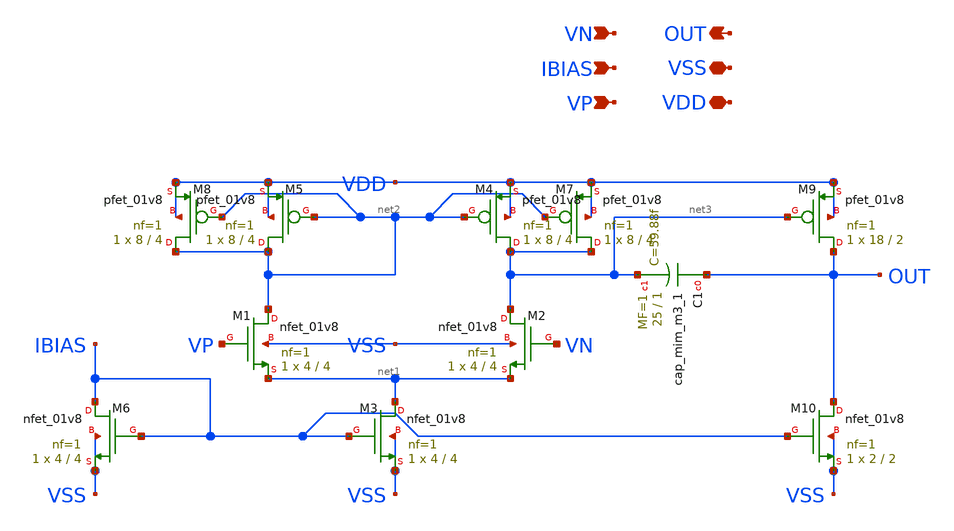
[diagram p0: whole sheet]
** sch_path: designs/libs/core_analog/core_bandgap/5t-ota/n-ota-bg.sch
**.subckt n-ota-bg VDD VSS IBIAS VP VN OUT
*.iopin VDD
*.iopin VSS
*.ipin IBIAS
*.ipin VP
*.ipin VN
*.opin OUT
XM1 net2 VP net1 VSS sky130_fd_pr__nfet_01v8 L=4 W=4 nf=1 ad='int((nf+1)/2) * W/nf * 0.29' as='int((nf+2)/2) * W/nf * 0.29'
+ pd='2*int((nf+1)/2) * (W/nf + 0.29)' ps='2*int((nf+2)/2) * (W/nf + 0.29)' nrd='0.29 / W' nrs='0.29 / W'
+ sa=0 sb=0 sd=0 mult=1 m=1
XM2 net3 VN net1 VSS sky130_fd_pr__nfet_01v8 L=4 W=4 nf=1 ad='int((nf+1)/2) * W/nf * 0.29' as='int((nf+2)/2) * W/nf * 0.29'
+ pd='2*int((nf+1)/2) * (W/nf + 0.29)' ps='2*int((nf+2)/2) * (W/nf + 0.29)' nrd='0.29 / W' nrs='0.29 / W'
+ sa=0 sb=0 sd=0 mult=1 m=1
XM3 net1 IBIAS VSS VSS sky130_fd_pr__nfet_01v8 L=4 W=4 nf=1 ad='int((nf+1)/2) * W/nf * 0.29' as='int((nf+2)/2) * W/nf * 0.29'
+ pd='2*int((nf+1)/2) * (W/nf + 0.29)' ps='2*int((nf+2)/2) * (W/nf + 0.29)' nrd='0.29 / W' nrs='0.29 / W'
+ sa=0 sb=0 sd=0 mult=1 m=1
XM4 net3 net2 VDD VDD sky130_fd_pr__pfet_01v8 L=4 W=8 nf=1 ad='int((nf+1)/2) * W/nf * 0.29' as='int((nf+2)/2) * W/nf * 0.29'
+ pd='2*int((nf+1)/2) * (W/nf + 0.29)' ps='2*int((nf+2)/2) * (W/nf + 0.29)' nrd='0.29 / W' nrs='0.29 / W'
+ sa=0 sb=0 sd=0 mult=1 m=1
XM5 net2 net2 VDD VDD sky130_fd_pr__pfet_01v8 L=4 W=8 nf=1 ad='int((nf+1)/2) * W/nf * 0.29' as='int((nf+2)/2) * W/nf * 0.29'
+ pd='2*int((nf+1)/2) * (W/nf + 0.29)' ps='2*int((nf+2)/2) * (W/nf + 0.29)' nrd='0.29 / W' nrs='0.29 / W'
+ sa=0 sb=0 sd=0 mult=1 m=1
XM6 IBIAS IBIAS VSS VSS sky130_fd_pr__nfet_01v8 L=4 W=4 nf=1 ad='int((nf+1)/2) * W/nf * 0.29' as='int((nf+2)/2) * W/nf * 0.29'
+ pd='2*int((nf+1)/2) * (W/nf + 0.29)' ps='2*int((nf+2)/2) * (W/nf + 0.29)' nrd='0.29 / W' nrs='0.29 / W'
+ sa=0 sb=0 sd=0 mult=1 m=1
XM7 net3 net2 VDD VDD sky130_fd_pr__pfet_01v8 L=4 W=8 nf=1 ad='int((nf+1)/2) * W/nf * 0.29' as='int((nf+2)/2) * W/nf * 0.29'
+ pd='2*int((nf+1)/2) * (W/nf + 0.29)' ps='2*int((nf+2)/2) * (W/nf + 0.29)' nrd='0.29 / W' nrs='0.29 / W'
+ sa=0 sb=0 sd=0 mult=1 m=1
XM8 net2 net2 VDD VDD sky130_fd_pr__pfet_01v8 L=4 W=8 nf=1 ad='int((nf+1)/2) * W/nf * 0.29' as='int((nf+2)/2) * W/nf * 0.29'
+ pd='2*int((nf+1)/2) * (W/nf + 0.29)' ps='2*int((nf+2)/2) * (W/nf + 0.29)' nrd='0.29 / W' nrs='0.29 / W'
+ sa=0 sb=0 sd=0 mult=1 m=1
XM9 OUT net3 VDD VDD sky130_fd_pr__pfet_01v8 L=2 W=18 nf=1 ad='int((nf+1)/2) * W/nf * 0.29' as='int((nf+2)/2) * W/nf * 0.29'
+ pd='2*int((nf+1)/2) * (W/nf + 0.29)' ps='2*int((nf+2)/2) * (W/nf + 0.29)' nrd='0.29 / W' nrs='0.29 / W'
+ sa=0 sb=0 sd=0 mult=1 m=1
XM10 OUT IBIAS VSS VSS sky130_fd_pr__nfet_01v8 L=2 W=2 nf=1 ad='int((nf+1)/2) * W/nf * 0.29' as='int((nf+2)/2) * W/nf * 0.29'
+ pd='2*int((nf+1)/2) * (W/nf + 0.29)' ps='2*int((nf+2)/2) * (W/nf + 0.29)' nrd='0.29 / W' nrs='0.29 / W'
+ sa=0 sb=0 sd=0 mult=1 m=1
XC1 OUT net3 sky130_fd_pr__cap_mim_m3_1 W=25 L=1 MF=1 m=1
**.ends
.end
